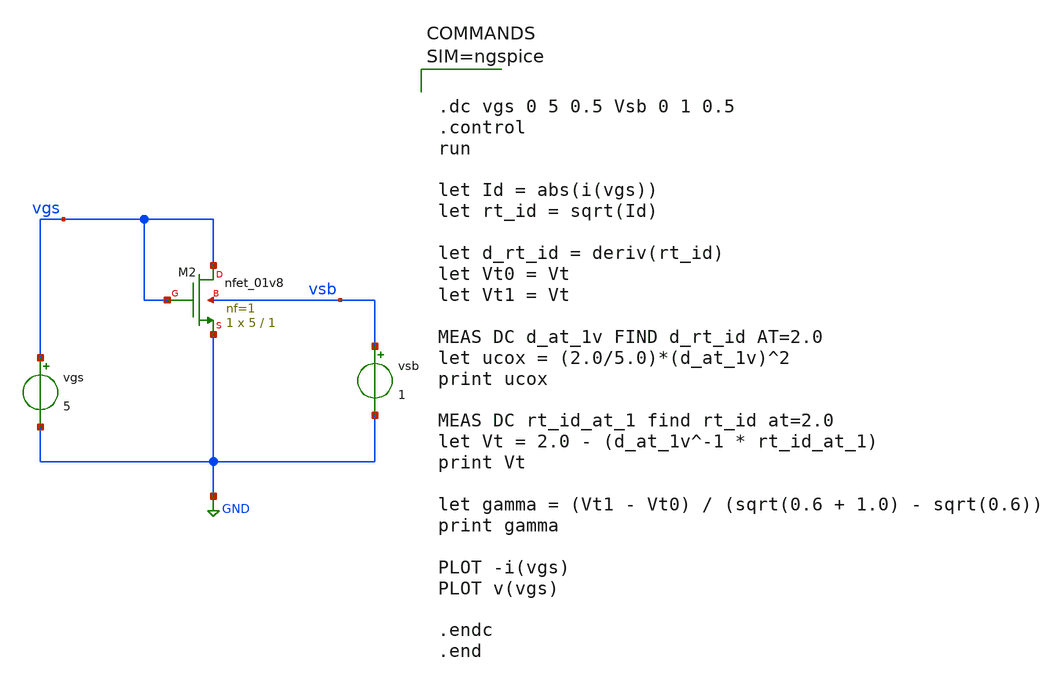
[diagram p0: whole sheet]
** sch_path: xschem/para.ex2.sch
**.subckt para.ex2
vsb vsb GND 1
vgs vgs GND 5
XM2 vgs vgs GND vsb sky130_fd_pr__nfet_01v8 L=1 W=5 nf=1 ad='int((1 + 1)/2) * 5 / 1 * 0.29' as='int((1 + 2)/2) * 5 / 1 * 0.29'
+ pd='2*int((1 + 1)/2) * (5 / 1 + 0.29)' ps='2*int((1 + 2)/2) * (5 / 1 + 0.29)' nrd='0.29 / 5 ' nrs='0.29 / 5 '
+ sa=0 sb=0 sd=0 mult=1 m=1
**** begin user architecture code

** opencircuitdesign pdks install
.lib $::SKYWATER_MODELS/sky130.lib.spice tt




.dc vgs 0 5 0.5 Vsb 0 1 0.5
.control
run

let Id = abs(i(vgs))
let rt_id = sqrt(Id)

let d_rt_id = deriv(rt_id)
let Vt0 = Vt
let Vt1 = Vt

MEAS DC d_at_1v FIND d_rt_id AT=2.0
let ucox = (2.0/5.0)*(d_at_1v)^2
print ucox

MEAS DC rt_id_at_1 find rt_id at=2.0
let Vt = 2.0 - (d_at_1v^-1 * rt_id_at_1)
print Vt

let gamma = (Vt1 - Vt0) / (sqrt(0.6 + 1.0) - sqrt(0.6))
print gamma

PLOT -i(vgs)
PLOT v(vgs)

.endc
.end



**** end user architecture code
**.ends
.GLOBAL GND
.end
